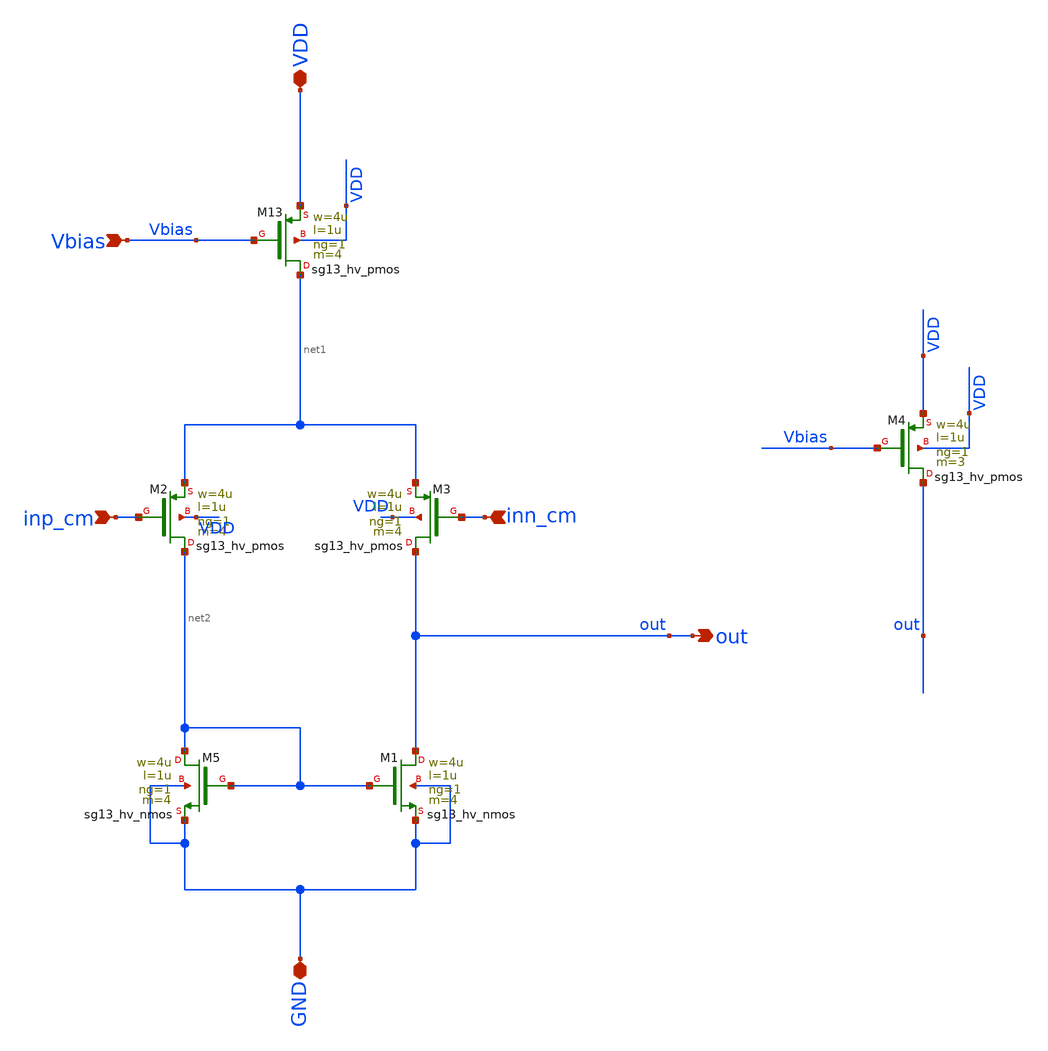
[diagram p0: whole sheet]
** sch_path: xschem/V2I/V2I_shift_final.sch
**.subckt V2I_shift_final inn_cm inp_cm out Vbias VDD GND
*.ipin inn_cm
*.ipin inp_cm
*.opin out
*.ipin Vbias
*.iopin VDD
*.iopin GND
XM2 net2 inp_cm net1 VDD sg13_hv_pmos w=4u l=1u ng=1 m=4 mm_ok=1
XM5 net2 net2 GND GND sg13_hv_nmos w=4u l=1u ng=1 m=4 mm_ok=1
XM13 net1 Vbias VDD VDD sg13_hv_pmos w=4u l=1u ng=1 m=4 mm_ok=1
XM1 out net2 GND GND sg13_hv_nmos w=4u l=1u ng=1 m=4 mm_ok=1
XM3 out inn_cm net1 VDD sg13_hv_pmos w=4u l=1u ng=1 m=4 mm_ok=1
XM4 out Vbias VDD VDD sg13_hv_pmos w=4u l=1u ng=1 m=3 mm_ok=1
**.ends
.end
